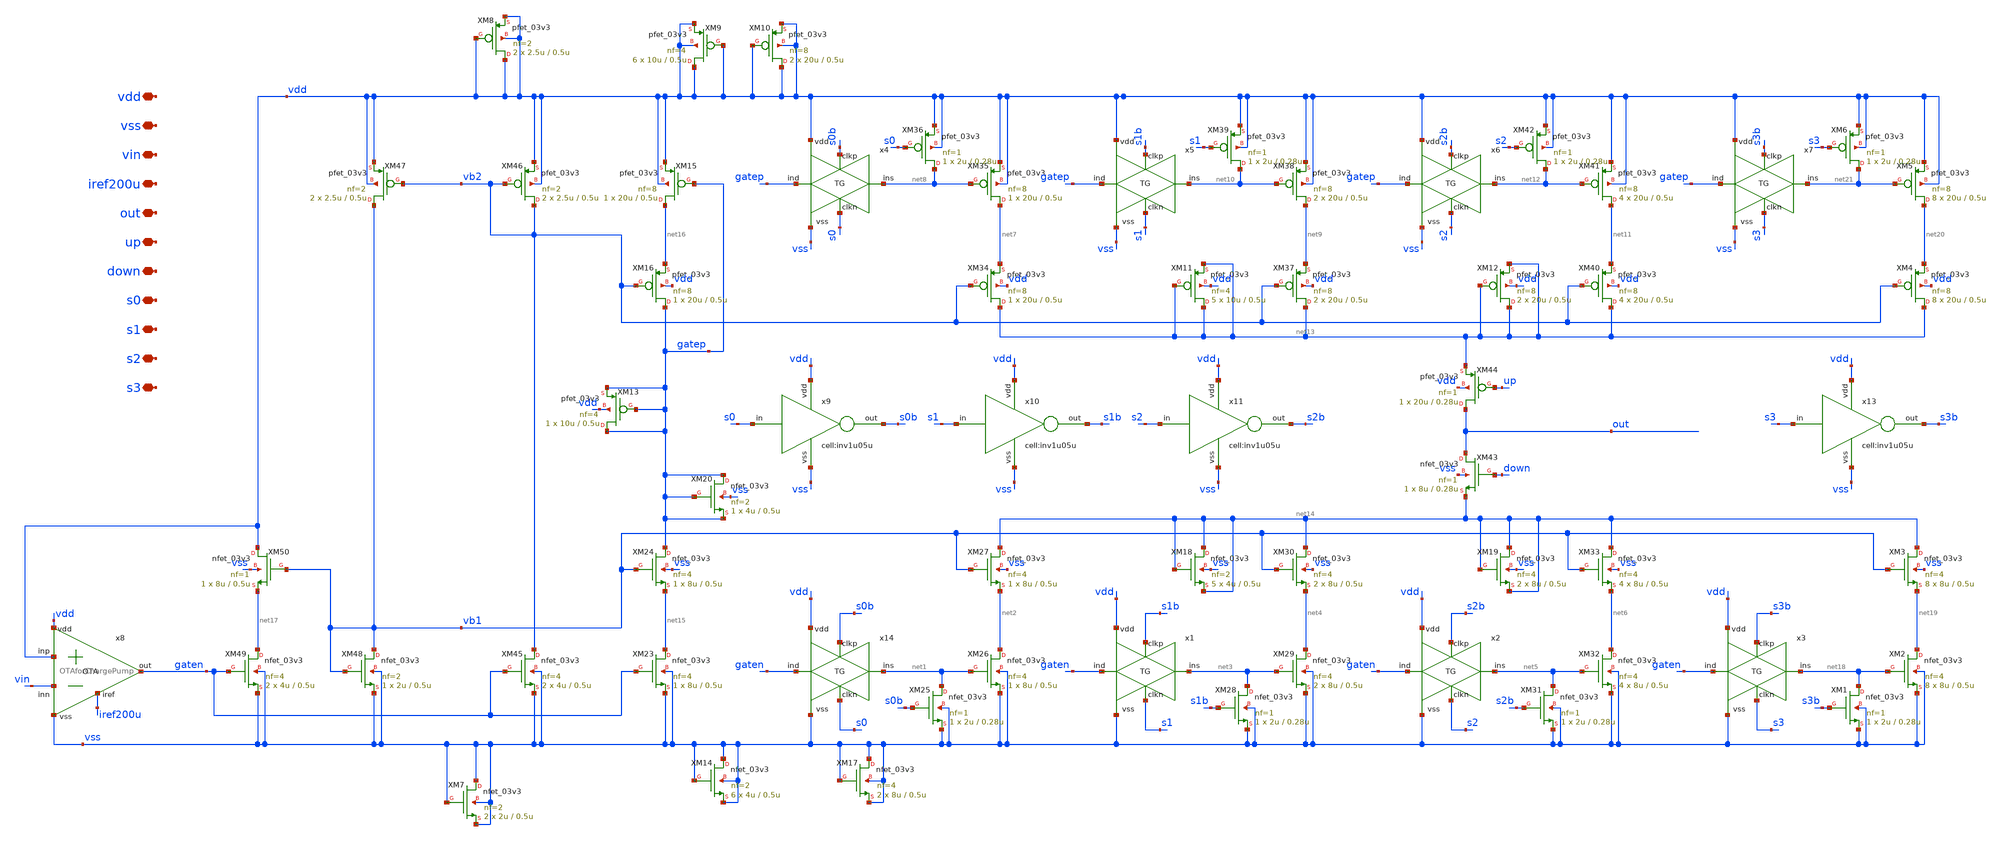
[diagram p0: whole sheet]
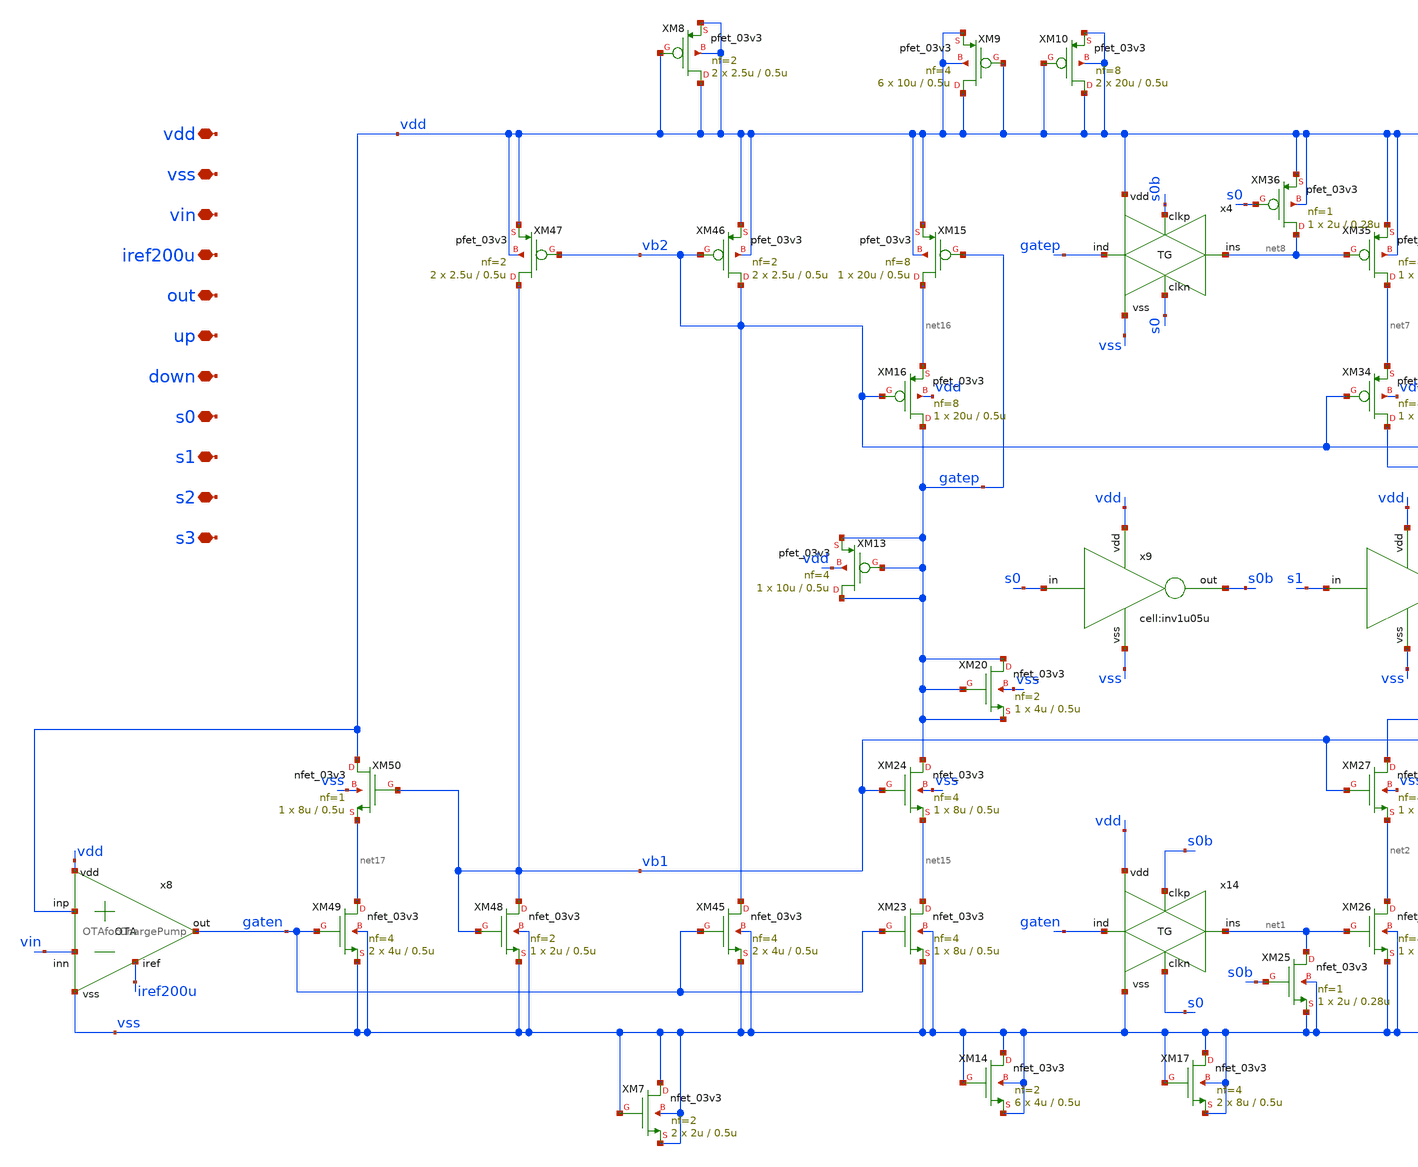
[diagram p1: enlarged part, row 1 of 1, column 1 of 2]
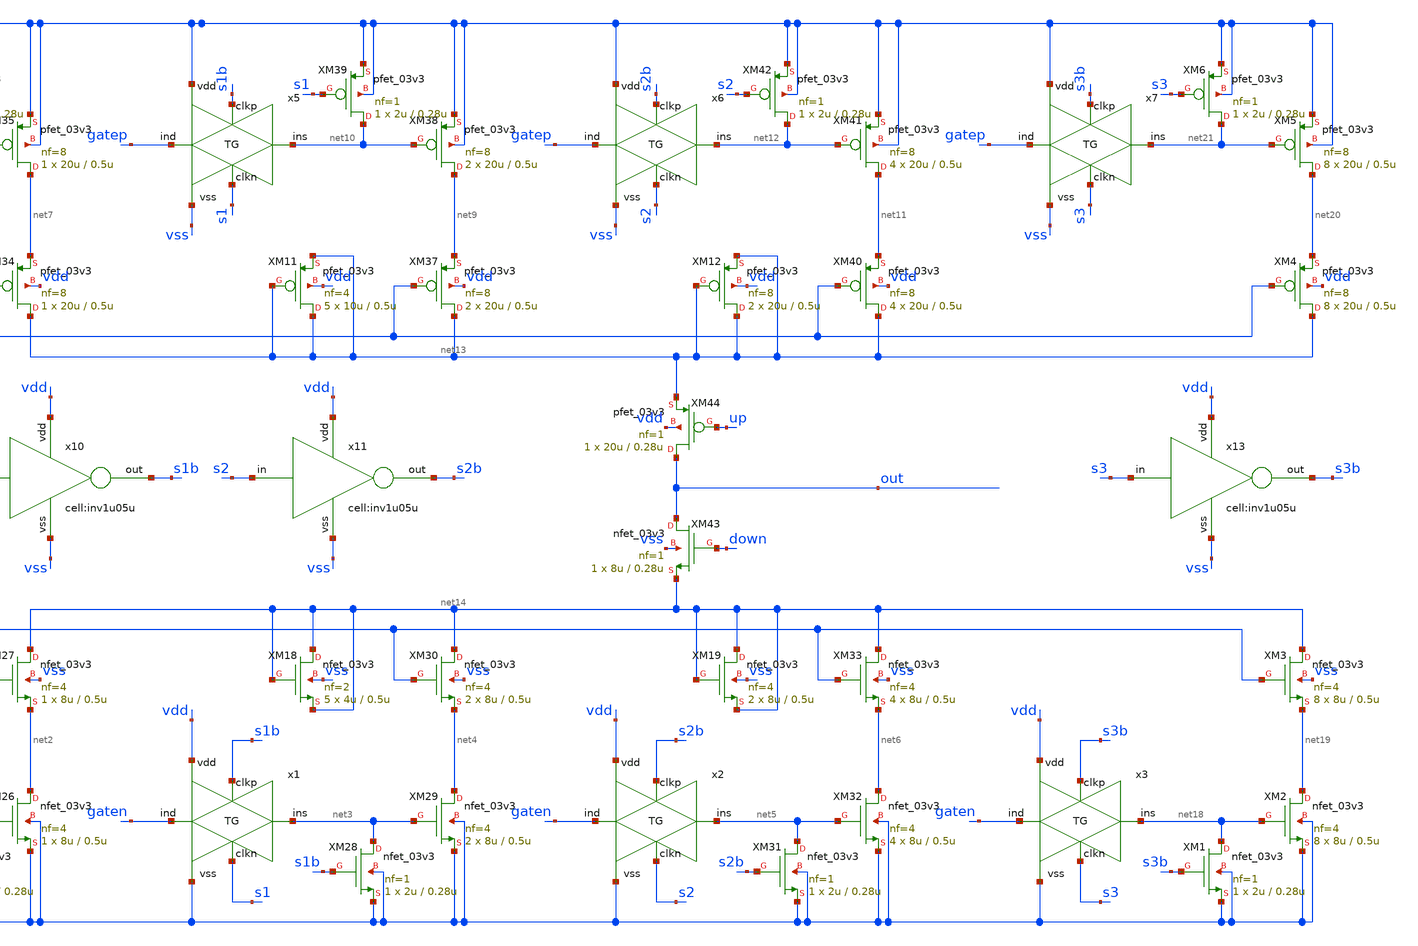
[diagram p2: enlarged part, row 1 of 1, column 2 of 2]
** sch_path: designs/libs/qw_core_analog/PCP1248Xflatten/PCP1248Xflatten.sch
**.subckt PCP1248Xflatten vdd vss vin iref200u out up down s0 s1 s2 s3
*.iopin vdd
*.iopin vss
*.iopin vin
*.iopin iref200u
*.iopin out
*.iopin up
*.iopin down
*.iopin s0
*.iopin s1
*.iopin s2
*.iopin s3
XM25 net1 s0b vss vss nfet_03v3 L=0.28u W=2u nf=1 ad='int((nf+1)/2) * W/nf * 0.18u' as='int((nf+2)/2) * W/nf * 0.18u'
+ pd='2*int((nf+1)/2) * (W/nf + 0.18u)' ps='2*int((nf+2)/2) * (W/nf + 0.18u)' nrd='0.18u / W' nrs='0.18u / W'
+ sa=0 sb=0 sd=0 m=1
XM26 net2 net1 vss vss nfet_03v3 L=0.5u W=8u nf=4 ad='int((nf+1)/2) * W/nf * 0.18u' as='int((nf+2)/2) * W/nf * 0.18u'
+ pd='2*int((nf+1)/2) * (W/nf + 0.18u)' ps='2*int((nf+2)/2) * (W/nf + 0.18u)' nrd='0.18u / W' nrs='0.18u / W'
+ sa=0 sb=0 sd=0 m=1
XM27 net14 vb1 net2 vss nfet_03v3 L=0.5u W=8u nf=4 ad='int((nf+1)/2) * W/nf * 0.18u' as='int((nf+2)/2) * W/nf * 0.18u'
+ pd='2*int((nf+1)/2) * (W/nf + 0.18u)' ps='2*int((nf+2)/2) * (W/nf + 0.18u)' nrd='0.18u / W' nrs='0.18u / W'
+ sa=0 sb=0 sd=0 m=1
XM28 net3 s1b vss vss nfet_03v3 L=0.28u W=2u nf=1 ad='int((nf+1)/2) * W/nf * 0.18u' as='int((nf+2)/2) * W/nf * 0.18u'
+ pd='2*int((nf+1)/2) * (W/nf + 0.18u)' ps='2*int((nf+2)/2) * (W/nf + 0.18u)' nrd='0.18u / W' nrs='0.18u / W'
+ sa=0 sb=0 sd=0 m=1
XM29 net4 net3 vss vss nfet_03v3 L=0.5u W=8u nf=4 ad='int((nf+1)/2) * W/nf * 0.18u' as='int((nf+2)/2) * W/nf * 0.18u'
+ pd='2*int((nf+1)/2) * (W/nf + 0.18u)' ps='2*int((nf+2)/2) * (W/nf + 0.18u)' nrd='0.18u / W' nrs='0.18u / W'
+ sa=0 sb=0 sd=0 m=2
XM30 net14 vb1 net4 vss nfet_03v3 L=0.5u W=8u nf=4 ad='int((nf+1)/2) * W/nf * 0.18u' as='int((nf+2)/2) * W/nf * 0.18u'
+ pd='2*int((nf+1)/2) * (W/nf + 0.18u)' ps='2*int((nf+2)/2) * (W/nf + 0.18u)' nrd='0.18u / W' nrs='0.18u / W'
+ sa=0 sb=0 sd=0 m=2
XM31 net5 s2b vss vss nfet_03v3 L=0.28u W=2u nf=1 ad='int((nf+1)/2) * W/nf * 0.18u' as='int((nf+2)/2) * W/nf * 0.18u'
+ pd='2*int((nf+1)/2) * (W/nf + 0.18u)' ps='2*int((nf+2)/2) * (W/nf + 0.18u)' nrd='0.18u / W' nrs='0.18u / W'
+ sa=0 sb=0 sd=0 m=1
XM32 net6 net5 vss vss nfet_03v3 L=0.5u W=8u nf=4 ad='int((nf+1)/2) * W/nf * 0.18u' as='int((nf+2)/2) * W/nf * 0.18u'
+ pd='2*int((nf+1)/2) * (W/nf + 0.18u)' ps='2*int((nf+2)/2) * (W/nf + 0.18u)' nrd='0.18u / W' nrs='0.18u / W'
+ sa=0 sb=0 sd=0 m=4
XM33 net14 vb1 net6 vss nfet_03v3 L=0.5u W=8u nf=4 ad='int((nf+1)/2) * W/nf * 0.18u' as='int((nf+2)/2) * W/nf * 0.18u'
+ pd='2*int((nf+1)/2) * (W/nf + 0.18u)' ps='2*int((nf+2)/2) * (W/nf + 0.18u)' nrd='0.18u / W' nrs='0.18u / W'
+ sa=0 sb=0 sd=0 m=4
XM34 net13 vb2 net7 vdd pfet_03v3 L=0.5u W=20u nf=8 ad='int((nf+1)/2) * W/nf * 0.18u' as='int((nf+2)/2) * W/nf * 0.18u'
+ pd='2*int((nf+1)/2) * (W/nf + 0.18u)' ps='2*int((nf+2)/2) * (W/nf + 0.18u)' nrd='0.18u / W' nrs='0.18u / W'
+ sa=0 sb=0 sd=0 m=1
XM35 net7 net8 vdd vdd pfet_03v3 L=0.5u W=20u nf=8 ad='int((nf+1)/2) * W/nf * 0.18u' as='int((nf+2)/2) * W/nf * 0.18u'
+ pd='2*int((nf+1)/2) * (W/nf + 0.18u)' ps='2*int((nf+2)/2) * (W/nf + 0.18u)' nrd='0.18u / W' nrs='0.18u / W'
+ sa=0 sb=0 sd=0 m=1
XM36 net8 s0 vdd vdd pfet_03v3 L=0.28u W=2u nf=1 ad='int((nf+1)/2) * W/nf * 0.18u' as='int((nf+2)/2) * W/nf * 0.18u'
+ pd='2*int((nf+1)/2) * (W/nf + 0.18u)' ps='2*int((nf+2)/2) * (W/nf + 0.18u)' nrd='0.18u / W' nrs='0.18u / W'
+ sa=0 sb=0 sd=0 m=1
XM37 net13 vb2 net9 vdd pfet_03v3 L=0.5u W=20u nf=8 ad='int((nf+1)/2) * W/nf * 0.18u' as='int((nf+2)/2) * W/nf * 0.18u'
+ pd='2*int((nf+1)/2) * (W/nf + 0.18u)' ps='2*int((nf+2)/2) * (W/nf + 0.18u)' nrd='0.18u / W' nrs='0.18u / W'
+ sa=0 sb=0 sd=0 m=2
XM38 net9 net10 vdd vdd pfet_03v3 L=0.5u W=20u nf=8 ad='int((nf+1)/2) * W/nf * 0.18u' as='int((nf+2)/2) * W/nf * 0.18u'
+ pd='2*int((nf+1)/2) * (W/nf + 0.18u)' ps='2*int((nf+2)/2) * (W/nf + 0.18u)' nrd='0.18u / W' nrs='0.18u / W'
+ sa=0 sb=0 sd=0 m=2
XM39 net10 s1 vdd vdd pfet_03v3 L=0.28u W=2u nf=1 ad='int((nf+1)/2) * W/nf * 0.18u' as='int((nf+2)/2) * W/nf * 0.18u'
+ pd='2*int((nf+1)/2) * (W/nf + 0.18u)' ps='2*int((nf+2)/2) * (W/nf + 0.18u)' nrd='0.18u / W' nrs='0.18u / W'
+ sa=0 sb=0 sd=0 m=1
XM40 net13 vb2 net11 vdd pfet_03v3 L=0.5u W=20u nf=8 ad='int((nf+1)/2) * W/nf * 0.18u' as='int((nf+2)/2) * W/nf * 0.18u'
+ pd='2*int((nf+1)/2) * (W/nf + 0.18u)' ps='2*int((nf+2)/2) * (W/nf + 0.18u)' nrd='0.18u / W' nrs='0.18u / W'
+ sa=0 sb=0 sd=0 m=4
XM41 net11 net12 vdd vdd pfet_03v3 L=0.5u W=20u nf=8 ad='int((nf+1)/2) * W/nf * 0.18u' as='int((nf+2)/2) * W/nf * 0.18u'
+ pd='2*int((nf+1)/2) * (W/nf + 0.18u)' ps='2*int((nf+2)/2) * (W/nf + 0.18u)' nrd='0.18u / W' nrs='0.18u / W'
+ sa=0 sb=0 sd=0 m=4
XM42 net12 s2 vdd vdd pfet_03v3 L=0.28u W=2u nf=1 ad='int((nf+1)/2) * W/nf * 0.18u' as='int((nf+2)/2) * W/nf * 0.18u'
+ pd='2*int((nf+1)/2) * (W/nf + 0.18u)' ps='2*int((nf+2)/2) * (W/nf + 0.18u)' nrd='0.18u / W' nrs='0.18u / W'
+ sa=0 sb=0 sd=0 m=1
XM43 out down net14 vss nfet_03v3 L=0.28u W=8u nf=1 ad='int((nf+1)/2) * W/nf * 0.18u' as='int((nf+2)/2) * W/nf * 0.18u'
+ pd='2*int((nf+1)/2) * (W/nf + 0.18u)' ps='2*int((nf+2)/2) * (W/nf + 0.18u)' nrd='0.18u / W' nrs='0.18u / W'
+ sa=0 sb=0 sd=0 m=1
XM44 out up net13 vdd pfet_03v3 L=0.28u W=20u nf=1 ad='int((nf+1)/2) * W/nf * 0.18u' as='int((nf+2)/2) * W/nf * 0.18u'
+ pd='2*int((nf+1)/2) * (W/nf + 0.18u)' ps='2*int((nf+2)/2) * (W/nf + 0.18u)' nrd='0.18u / W' nrs='0.18u / W'
+ sa=0 sb=0 sd=0 m=1
XM15 net16 gatep vdd vdd pfet_03v3 L=0.5u W=20u nf=8 ad='int((nf+1)/2) * W/nf * 0.18u' as='int((nf+2)/2) * W/nf * 0.18u'
+ pd='2*int((nf+1)/2) * (W/nf + 0.18u)' ps='2*int((nf+2)/2) * (W/nf + 0.18u)' nrd='0.18u / W' nrs='0.18u / W'
+ sa=0 sb=0 sd=0 m=1
XM16 gatep vb2 net16 vdd pfet_03v3 L=0.5u W=20u nf=8 ad='int((nf+1)/2) * W/nf * 0.18u' as='int((nf+2)/2) * W/nf * 0.18u'
+ pd='2*int((nf+1)/2) * (W/nf + 0.18u)' ps='2*int((nf+2)/2) * (W/nf + 0.18u)' nrd='0.18u / W' nrs='0.18u / W'
+ sa=0 sb=0 sd=0 m=1
XM23 net15 gaten vss vss nfet_03v3 L=0.5u W=8u nf=4 ad='int((nf+1)/2) * W/nf * 0.18u' as='int((nf+2)/2) * W/nf * 0.18u'
+ pd='2*int((nf+1)/2) * (W/nf + 0.18u)' ps='2*int((nf+2)/2) * (W/nf + 0.18u)' nrd='0.18u / W' nrs='0.18u / W'
+ sa=0 sb=0 sd=0 m=1
XM24 gatep vb1 net15 vss nfet_03v3 L=0.5u W=8u nf=4 ad='int((nf+1)/2) * W/nf * 0.18u' as='int((nf+2)/2) * W/nf * 0.18u'
+ pd='2*int((nf+1)/2) * (W/nf + 0.18u)' ps='2*int((nf+2)/2) * (W/nf + 0.18u)' nrd='0.18u / W' nrs='0.18u / W'
+ sa=0 sb=0 sd=0 m=1
XM45 vb2 gaten vss vss nfet_03v3 L=0.5u W=4u nf=4 ad='int((nf+1)/2) * W/nf * 0.18u' as='int((nf+2)/2) * W/nf * 0.18u'
+ pd='2*int((nf+1)/2) * (W/nf + 0.18u)' ps='2*int((nf+2)/2) * (W/nf + 0.18u)' nrd='0.18u / W' nrs='0.18u / W'
+ sa=0 sb=0 sd=0 m=2
XM46 vb2 vb2 vdd vdd pfet_03v3 L=0.5u W=2.5u nf=2 ad='int((nf+1)/2) * W/nf * 0.18u' as='int((nf+2)/2) * W/nf * 0.18u'
+ pd='2*int((nf+1)/2) * (W/nf + 0.18u)' ps='2*int((nf+2)/2) * (W/nf + 0.18u)' nrd='0.18u / W' nrs='0.18u / W'
+ sa=0 sb=0 sd=0 m=2
XM47 vb1 vb2 vdd vdd pfet_03v3 L=0.5u W=2.5u nf=2 ad='int((nf+1)/2) * W/nf * 0.18u' as='int((nf+2)/2) * W/nf * 0.18u'
+ pd='2*int((nf+1)/2) * (W/nf + 0.18u)' ps='2*int((nf+2)/2) * (W/nf + 0.18u)' nrd='0.18u / W' nrs='0.18u / W'
+ sa=0 sb=0 sd=0 m=2
XM48 vb1 vb1 vss vss nfet_03v3 L=0.5u W=2u nf=2 ad='int((nf+1)/2) * W/nf * 0.18u' as='int((nf+2)/2) * W/nf * 0.18u'
+ pd='2*int((nf+1)/2) * (W/nf + 0.18u)' ps='2*int((nf+2)/2) * (W/nf + 0.18u)' nrd='0.18u / W' nrs='0.18u / W'
+ sa=0 sb=0 sd=0 m=1
XM49 net17 gaten vss vss nfet_03v3 L=0.5u W=4u nf=4 ad='int((nf+1)/2) * W/nf * 0.18u' as='int((nf+2)/2) * W/nf * 0.18u'
+ pd='2*int((nf+1)/2) * (W/nf + 0.18u)' ps='2*int((nf+2)/2) * (W/nf + 0.18u)' nrd='0.18u / W' nrs='0.18u / W'
+ sa=0 sb=0 sd=0 m=2
XM50 vdd vb1 net17 vss nfet_03v3 L=0.5u W=8u nf=1 ad='int((nf+1)/2) * W/nf * 0.18u' as='int((nf+2)/2) * W/nf * 0.18u'
+ pd='2*int((nf+1)/2) * (W/nf + 0.18u)' ps='2*int((nf+2)/2) * (W/nf + 0.18u)' nrd='0.18u / W' nrs='0.18u / W'
+ sa=0 sb=0 sd=0 m=1
x8 vdd iref200u vdd vin gaten vss OTAforChargePump
x9 s0 vdd s0b vss inv1u05u
x10 s1 vdd s1b vss inv1u05u
x11 s2 vdd s2b vss inv1u05u
XM1 net18 s3b vss vss nfet_03v3 L=0.28u W=2u nf=1 ad='int((nf+1)/2) * W/nf * 0.18u' as='int((nf+2)/2) * W/nf * 0.18u'
+ pd='2*int((nf+1)/2) * (W/nf + 0.18u)' ps='2*int((nf+2)/2) * (W/nf + 0.18u)' nrd='0.18u / W' nrs='0.18u / W'
+ sa=0 sb=0 sd=0 m=1
XM2 net19 net18 vss vss nfet_03v3 L=0.5u W=8u nf=4 ad='int((nf+1)/2) * W/nf * 0.18u' as='int((nf+2)/2) * W/nf * 0.18u'
+ pd='2*int((nf+1)/2) * (W/nf + 0.18u)' ps='2*int((nf+2)/2) * (W/nf + 0.18u)' nrd='0.18u / W' nrs='0.18u / W'
+ sa=0 sb=0 sd=0 m=8
XM3 net14 vb1 net19 vss nfet_03v3 L=0.5u W=8u nf=4 ad='int((nf+1)/2) * W/nf * 0.18u' as='int((nf+2)/2) * W/nf * 0.18u'
+ pd='2*int((nf+1)/2) * (W/nf + 0.18u)' ps='2*int((nf+2)/2) * (W/nf + 0.18u)' nrd='0.18u / W' nrs='0.18u / W'
+ sa=0 sb=0 sd=0 m=8
XM4 net13 vb2 net20 vdd pfet_03v3 L=0.5u W=20u nf=8 ad='int((nf+1)/2) * W/nf * 0.18u' as='int((nf+2)/2) * W/nf * 0.18u'
+ pd='2*int((nf+1)/2) * (W/nf + 0.18u)' ps='2*int((nf+2)/2) * (W/nf + 0.18u)' nrd='0.18u / W' nrs='0.18u / W'
+ sa=0 sb=0 sd=0 m=8
XM5 net20 net21 vdd vdd pfet_03v3 L=0.5u W=20u nf=8 ad='int((nf+1)/2) * W/nf * 0.18u' as='int((nf+2)/2) * W/nf * 0.18u'
+ pd='2*int((nf+1)/2) * (W/nf + 0.18u)' ps='2*int((nf+2)/2) * (W/nf + 0.18u)' nrd='0.18u / W' nrs='0.18u / W'
+ sa=0 sb=0 sd=0 m=8
XM6 net21 s3 vdd vdd pfet_03v3 L=0.28u W=2u nf=1 ad='int((nf+1)/2) * W/nf * 0.18u' as='int((nf+2)/2) * W/nf * 0.18u'
+ pd='2*int((nf+1)/2) * (W/nf + 0.18u)' ps='2*int((nf+2)/2) * (W/nf + 0.18u)' nrd='0.18u / W' nrs='0.18u / W'
+ sa=0 sb=0 sd=0 m=1
x13 s3 vdd s3b vss inv1u05u
XM7 vss vss vss vss nfet_03v3 L=0.5u W=2u nf=2 ad='int((nf+1)/2) * W/nf * 0.18u' as='int((nf+2)/2) * W/nf * 0.18u'
+ pd='2*int((nf+1)/2) * (W/nf + 0.18u)' ps='2*int((nf+2)/2) * (W/nf + 0.18u)' nrd='0.18u / W' nrs='0.18u / W'
+ sa=0 sb=0 sd=0 m=2
XM8 vdd vdd vdd vdd pfet_03v3 L=0.5u W=2.5u nf=2 ad='int((nf+1)/2) * W/nf * 0.18u' as='int((nf+2)/2) * W/nf * 0.18u'
+ pd='2*int((nf+1)/2) * (W/nf + 0.18u)' ps='2*int((nf+2)/2) * (W/nf + 0.18u)' nrd='0.18u / W' nrs='0.18u / W'
+ sa=0 sb=0 sd=0 m=2
XM9 vdd vdd vdd vdd pfet_03v3 L=0.5u W=10u nf=4 ad='int((nf+1)/2) * W/nf * 0.18u' as='int((nf+2)/2) * W/nf * 0.18u'
+ pd='2*int((nf+1)/2) * (W/nf + 0.18u)' ps='2*int((nf+2)/2) * (W/nf + 0.18u)' nrd='0.18u / W' nrs='0.18u / W'
+ sa=0 sb=0 sd=0 m=6
XM10 vdd vdd vdd vdd pfet_03v3 L=0.5u W=20u nf=8 ad='int((nf+1)/2) * W/nf * 0.18u' as='int((nf+2)/2) * W/nf * 0.18u'
+ pd='2*int((nf+1)/2) * (W/nf + 0.18u)' ps='2*int((nf+2)/2) * (W/nf + 0.18u)' nrd='0.18u / W' nrs='0.18u / W'
+ sa=0 sb=0 sd=0 m=2
XM11 net13 net13 net13 vdd pfet_03v3 L=0.5u W=10u nf=4 ad='int((nf+1)/2) * W/nf * 0.18u' as='int((nf+2)/2) * W/nf * 0.18u'
+ pd='2*int((nf+1)/2) * (W/nf + 0.18u)' ps='2*int((nf+2)/2) * (W/nf + 0.18u)' nrd='0.18u / W' nrs='0.18u / W'
+ sa=0 sb=0 sd=0 m=5
XM12 net13 net13 net13 vdd pfet_03v3 L=0.5u W=20u nf=8 ad='int((nf+1)/2) * W/nf * 0.18u' as='int((nf+2)/2) * W/nf * 0.18u'
+ pd='2*int((nf+1)/2) * (W/nf + 0.18u)' ps='2*int((nf+2)/2) * (W/nf + 0.18u)' nrd='0.18u / W' nrs='0.18u / W'
+ sa=0 sb=0 sd=0 m=2
XM13 gatep gatep gatep vdd pfet_03v3 L=0.5u W=10u nf=4 ad='int((nf+1)/2) * W/nf * 0.18u' as='int((nf+2)/2) * W/nf * 0.18u'
+ pd='2*int((nf+1)/2) * (W/nf + 0.18u)' ps='2*int((nf+2)/2) * (W/nf + 0.18u)' nrd='0.18u / W' nrs='0.18u / W'
+ sa=0 sb=0 sd=0 m=1
XM14 vss vss vss vss nfet_03v3 L=0.5u W=4u nf=2 ad='int((nf+1)/2) * W/nf * 0.18u' as='int((nf+2)/2) * W/nf * 0.18u'
+ pd='2*int((nf+1)/2) * (W/nf + 0.18u)' ps='2*int((nf+2)/2) * (W/nf + 0.18u)' nrd='0.18u / W' nrs='0.18u / W'
+ sa=0 sb=0 sd=0 m=6
XM17 vss vss vss vss nfet_03v3 L=0.5u W=8u nf=4 ad='int((nf+1)/2) * W/nf * 0.18u' as='int((nf+2)/2) * W/nf * 0.18u'
+ pd='2*int((nf+1)/2) * (W/nf + 0.18u)' ps='2*int((nf+2)/2) * (W/nf + 0.18u)' nrd='0.18u / W' nrs='0.18u / W'
+ sa=0 sb=0 sd=0 m=2
XM18 net14 net14 net14 vss nfet_03v3 L=0.5u W=4u nf=2 ad='int((nf+1)/2) * W/nf * 0.18u' as='int((nf+2)/2) * W/nf * 0.18u'
+ pd='2*int((nf+1)/2) * (W/nf + 0.18u)' ps='2*int((nf+2)/2) * (W/nf + 0.18u)' nrd='0.18u / W' nrs='0.18u / W'
+ sa=0 sb=0 sd=0 m=5
XM19 net14 net14 net14 vss nfet_03v3 L=0.5u W=8u nf=4 ad='int((nf+1)/2) * W/nf * 0.18u' as='int((nf+2)/2) * W/nf * 0.18u'
+ pd='2*int((nf+1)/2) * (W/nf + 0.18u)' ps='2*int((nf+2)/2) * (W/nf + 0.18u)' nrd='0.18u / W' nrs='0.18u / W'
+ sa=0 sb=0 sd=0 m=2
XM20 gatep gatep gatep vss nfet_03v3 L=0.5u W=4u nf=2 ad='int((nf+1)/2) * W/nf * 0.18u' as='int((nf+2)/2) * W/nf * 0.18u'
+ pd='2*int((nf+1)/2) * (W/nf + 0.18u)' ps='2*int((nf+2)/2) * (W/nf + 0.18u)' nrd='0.18u / W' nrs='0.18u / W'
+ sa=0 sb=0 sd=0 m=1
x14 vdd s0b gaten net1 vss s0 TG
x1 vdd s1b gaten net3 vss s1 TG
x2 vdd s2b gaten net5 vss s2 TG
x3 vdd s3b gaten net18 vss s3 TG
x4 vdd s0b gatep net8 vss s0 TG
x5 vdd s1b gatep net10 vss s1 TG
x6 vdd s2b gatep net12 vss s2 TG
x7 vdd s3b gatep net21 vss s3 TG
**.ends
.end
